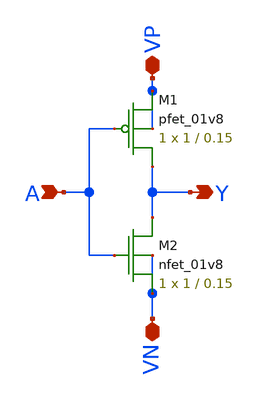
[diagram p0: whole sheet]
** sch_path: DRAM_Components/Schematic/inverter.sch
**.subckt inverter A VP Y VN
*.ipin A
*.iopin VP
*.opin Y
*.iopin VN
XM1 Y A VP VP sky130_fd_pr__pfet_01v8 L=0.15 W=1 nf=1 ad='int((nf+1)/2) * W/nf * 0.29' as='int((nf+2)/2) * W/nf * 0.29'
+ pd='2*int((nf+1)/2) * (W/nf + 0.29)' ps='2*int((nf+2)/2) * (W/nf + 0.29)' nrd='0.29 / W' nrs='0.29 / W'
+ sa=0 sb=0 sd=0 mult=1 m=1
XM2 Y A VN VN sky130_fd_pr__nfet_01v8 L=0.15 W=1 nf=1 ad='int((nf+1)/2) * W/nf * 0.29' as='int((nf+2)/2) * W/nf * 0.29'
+ pd='2*int((nf+1)/2) * (W/nf + 0.29)' ps='2*int((nf+2)/2) * (W/nf + 0.29)' nrd='0.29 / W' nrs='0.29 / W'
+ sa=0 sb=0 sd=0 mult=1 m=1
**.ends
.end
